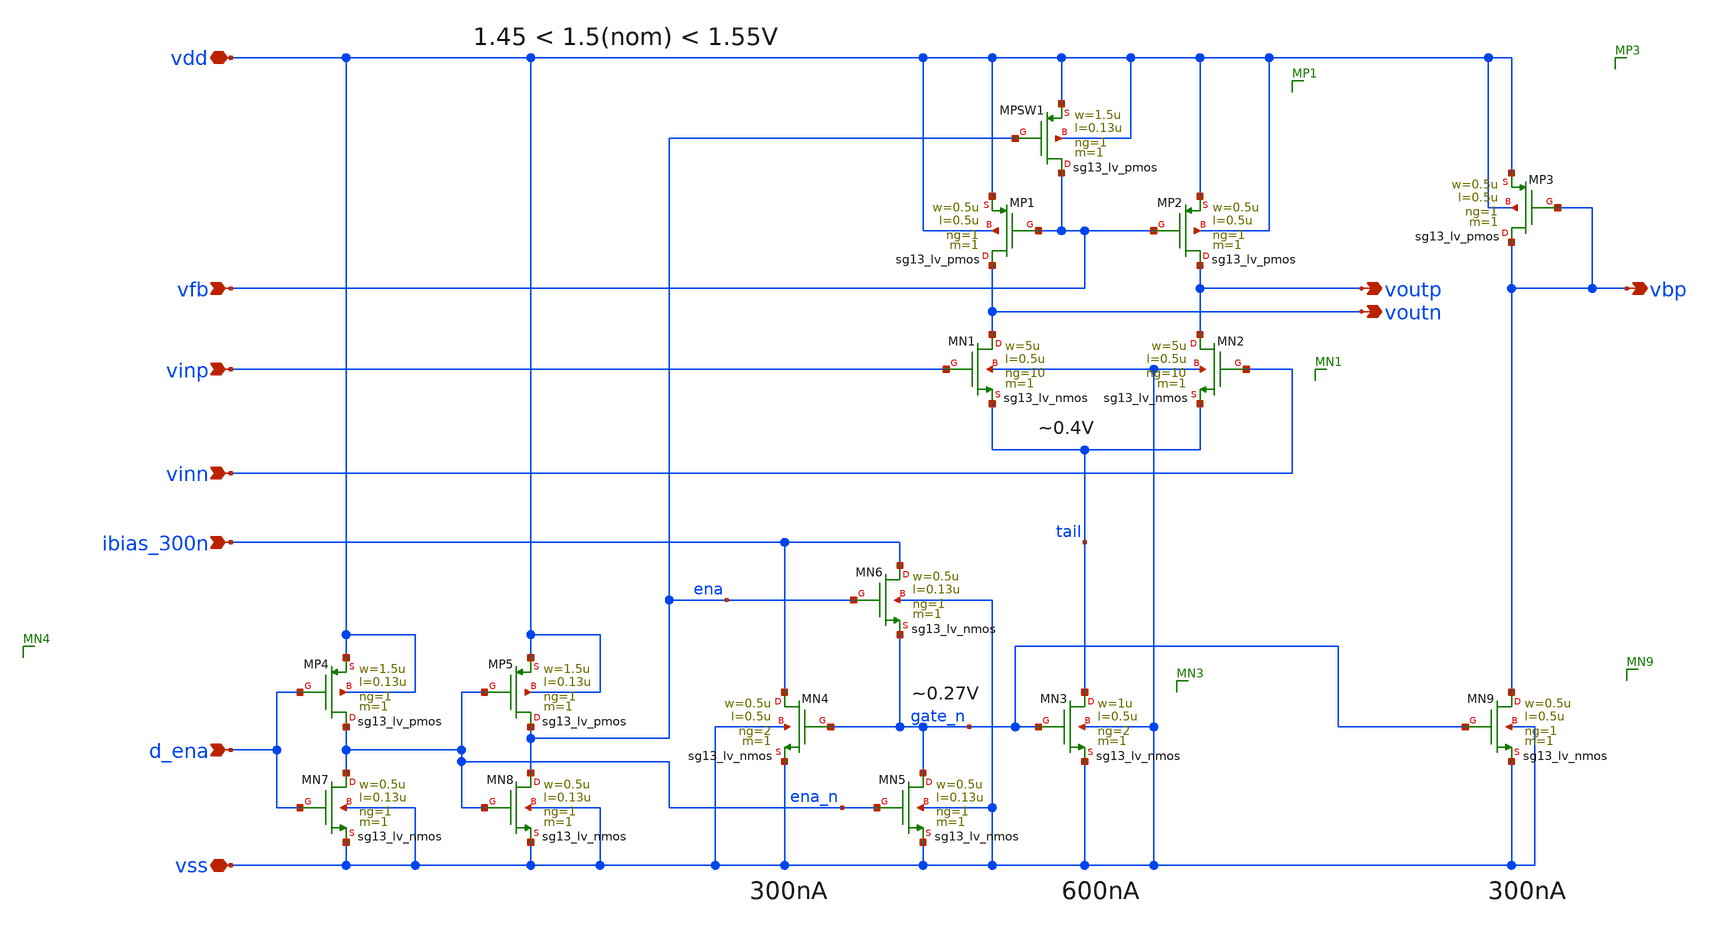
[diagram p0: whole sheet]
** sch_path: xschem/ota-5t-fd.sch
* (c) 2025 M. Koefinger
**.subckt ota-5t-fd ibias_300n vdd vss vinp vinn voutn d_ena voutp vfb vbp
*.ipin ibias_300n
*.iopin vdd
*.iopin vss
*.ipin vinp
*.ipin vinn
*.opin voutn
*.ipin d_ena
*.opin voutp
*.ipin vfb
*.opin vbp
XMN3 tail gate_n vss vss sg13_lv_nmos w=1u l=0.5u ng=2 m=1 mm_ok=1
XMP2 voutp vfb vdd vdd sg13_lv_pmos w=0.5u l=0.5u ng=1 m=1 mm_ok=1
XMN1 voutn vinp tail vss sg13_lv_nmos w=5u l=0.5u ng=10 m=1 mm_ok=1
XMN2 voutp vinn tail vss sg13_lv_nmos w=5u l=0.5u ng=10 m=1 mm_ok=1
XMP1 voutn vfb vdd vdd sg13_lv_pmos w=0.5u l=0.5u ng=1 m=1 mm_ok=1
XMN4 ibias_300n gate_n vss vss sg13_lv_nmos w=0.5u l=0.5u ng=2 m=1 mm_ok=1
XMN5 gate_n ena_n vss vss sg13_lv_nmos w=0.5u l=0.13u ng=1 m=1 mm_ok=1
XMPSW1 vfb ena vdd vdd sg13_lv_pmos w=1.5u l=0.13u ng=1 m=1 mm_ok=1
XMN8 ena ena_n vss vss sg13_lv_nmos w=0.5u l=0.13u ng=1 m=1 mm_ok=1
XMP5 ena ena_n vdd vdd sg13_lv_pmos w=1.5u l=0.13u ng=1 m=1 mm_ok=1
XMN6 ibias_300n ena gate_n vss sg13_lv_nmos w=0.5u l=0.13u ng=1 m=1 mm_ok=1
XMN7 ena_n d_ena vss vss sg13_lv_nmos w=0.5u l=0.13u ng=1 m=1 mm_ok=1
XMP4 ena_n d_ena vdd vdd sg13_lv_pmos w=1.5u l=0.13u ng=1 m=1 mm_ok=1
XMN9 vbp gate_n vss vss sg13_lv_nmos w=0.5u l=0.5u ng=1 m=1 mm_ok=1
XMP3 vbp vbp vdd vdd sg13_lv_pmos w=0.5u l=0.5u ng=1 m=1 mm_ok=1
**.ends
.end
